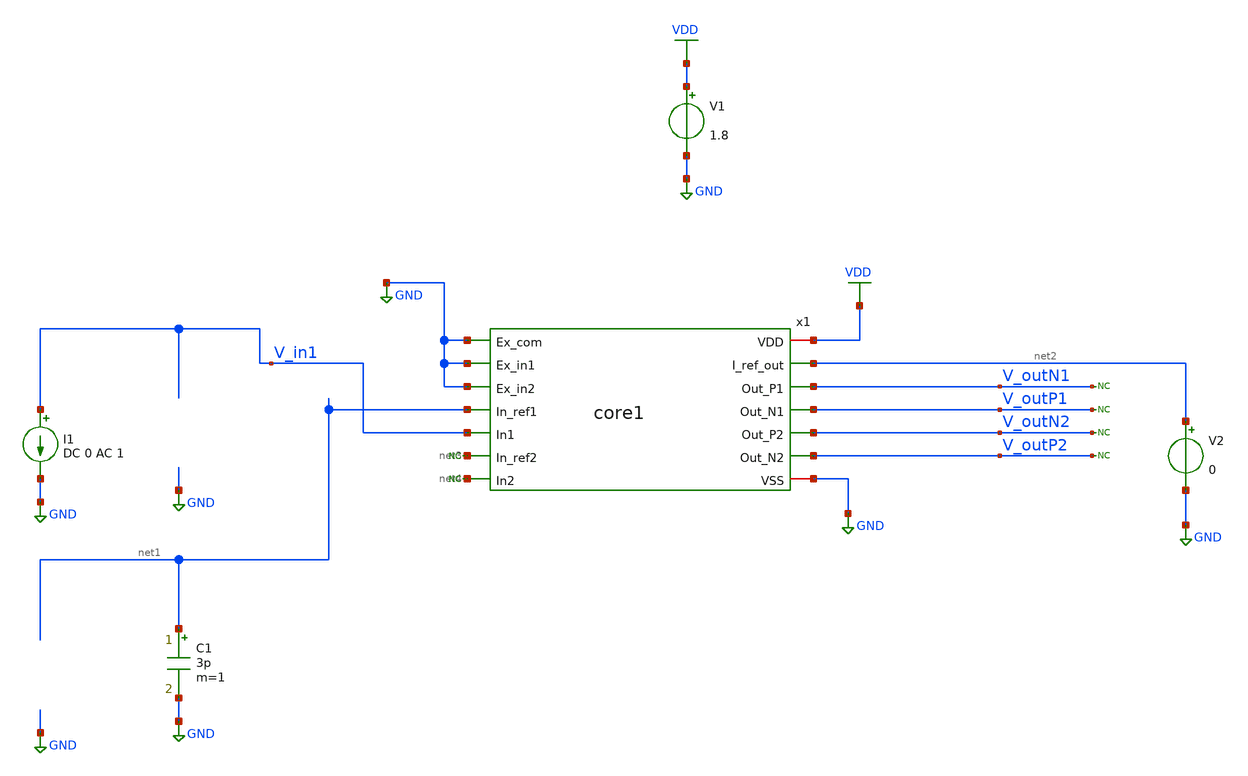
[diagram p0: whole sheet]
** sch_path: xschem/test_core1.sch
**.subckt test_core1
V1 VDD GND 1.8
I1 V_in1 GND DC 0 AC 1
x1 VDD GND GND GND net2 net1 V_outN1 V_in1 V_outP1 net3 V_outN2 net4 V_outP2 GND core1
C1 net1 GND 3p m=1
V2 net2 GND 0
* noconn V_outN1
* noconn V_outP1
* noconn V_outN2
* noconn V_outP2
* noconn #net4
* noconn #net3
**** begin user architecture code


*.options savecurrents
.option warn=1
.option temp=20
.control
set wr_vecnames
set wr_singlescale
set hcopydevtype=svg
** TIA



* save @m.xtia.xm1.msky130_fd_pr__nfet_01v8_lvt[gm]
* save @m.xtia.xm7.msky130_fd_pr__nfet_01v8_lvt[gm]
* save @m.xtia.xm17.msky130_fd_pr__nfet_01v8_lvt[gm]
* save @m.xtia.xm16.msky130_fd_pr__pfet_01v8[gm]
* save @m.xtia.xm8.msky130_fd_pr__pfet_01v8[gm]

* save @m.xtia.xm7.msky130_fd_pr__nfet_01v8_lvt[gm]
* save @m.xtia.xm8.msky130_fd_pr__pfet_01v8[gm]
save all
op

run
write test_core1.raw
reset
save all
ac dec 10 10 1T
plot v(V_in1)
plot v(V_in2)


plot db(v(V_outP1)-v(V_outN1))
*plot db(v(V_outP2)-v(V_outN2))


*meas ac gain FIND vdb(vtia_outp_1) AT=10MEG
*meas ac max_gain max vdb(vtia_outp_1) from=1MEG to=100G
*meas ac min_gain min vdb(vtia_outp_1) from=1MEG to=100MEG
*let bw_gain=gain-3
*meas ac bandwidth when vdb(vtia_outp_1)=bw_gain fall = LAST
*wrdata result_ac_tia.csv gain max_gain min_gain bandwidth


noise v(V_outP1, V_outN1) i1 dec 10 10 4G
print all
* wrdata result_noise.csv inoise_total onoise_total
setplot noise1
plot inoise_spectrum
plot onoise_spectrum
* hardcopy tia_rgc_inoise_spectrum.svg inoise_spectrum
* hardcopy tia_rgc_onoise_spectrum.svg onoise_spectrum
* plot log(inoise_spectrum)
* write noise_tia2.raw

noise v(V_outP1, V_outN1) i1 dec 10 1MEG 4G
print all
* wrdata result_noise.csv inoise_total onoise_total
setplot noise3
plot inoise_spectrum
plot onoise_spectrum
* hardcopy tia_rgc_inoise_spectrum_zoom.svg inoise_spectrum
* hardcopy tia_rgc_onoise_spectrum_zoom.svg onoise_spectrum
* plot log(inoise_spectrum)
* write noise_tia2.raw

noise v(V_outP1, V_outN1) i1 dec 10 100MEG 1.2G
print all
* wrdata result_noise.csv inoise_total onoise_total
setplot noise3
plot inoise_spectrum
plot onoise_spectrum

.endc




* .include ../../tia.spice
* .include ../../filter_diff.spice
* .include ../../cmm_sense3.spice

.include core1.spice
.include tiaA.spice
.include current_mirror_channel.spice
.include current_mirror_channel_s.spice
.include low_pvt_source.spice
.include outdriver_50ohm.spice



* .lib $::SKYWATER_MODELS/sky130.lib.spice #model#
* .lib $::SKYWATER_MODELS/sky130.lib.spice sf
.lib $::SKYWATER_MODELS/sky130.lib.spice.tt.red tt

**** end user architecture code
**.ends

* expanding   symbol:  core1.sym # of pins=14
** sym_path: xschem/core1.sym
** sch_path: xschem/core1.sch
.subckt core1 VDD Ex_com Ex_in1 Ex_in2 I_ref_out In_ref1 Out_P1 In1 Out_N1 In_ref2 Out_P2 In2 Out_N2
+ VSS
*.ipin In_ref1
*.iopin VDD
*.opin Out_N1
*.iopin VSS
*.ipin In2
*.opin Out_P1
*.opin Out_N2
*.opin Out_P2
*.opin I_ref_out
*.ipin In1
*.ipin In_ref2
*.ipin Ex_com
*.ipin Ex_in1
*.ipin Ex_in2
x1 VDD Out_P1 Out_N1 bias_outd_1 tia_out1 tia_ref_out1 VSS outdriver_50ohm
x2 net6 tia_out1 tia_filt_out1 net2 net3 tia_filt_out1 tia_ref_out1 bias_tia_1 VSS tiaA
x3 VDD tia_out2 tia_filt_out2 net4 net5 tia_filt_out2 tia_ref_out2 bias_tia_2 VSS tiaA
x4 VDD Out_P2 Out_N2 bias_outd_2 tia_out2 tia_ref_out2 VSS outdriver_50ohm
x5 VDD is_out bias_outd_2 I_ref_out bias_tia_2 current_mirror_channel_s
x6 VDD is_out bias_outd_1 net1 bias_tia_1 current_mirror_channel
x7 VDD is_out VSS low_pvt_source
* noconn #net1
R1 net2 In_ref1 sky130_fd_pr__res_generic_m5 W=20 L=5 m=1
R2 In1 net3 sky130_fd_pr__res_generic_m5 W=20 L=5 m=1
R3 net4 In_ref2 sky130_fd_pr__res_generic_m5 W=20 L=5 m=1
R4 In2 net5 sky130_fd_pr__res_generic_m5 W=20 L=5 m=1
V1 VDD net6 0
.ends


* expanding   symbol:  outdriver/outdriver_50ohm.sym # of pins=7
** sym_path: xschem/outdriver/outdriver_50ohm.sym
** sch_path: xschem/outdriver/outdriver_50ohm.sch
.subckt outdriver_50ohm VP OutP OutN I_Bias InputSignal InputRef VN
*.iopin VN
*.ipin InputRef
*.iopin VP
*.ipin I_Bias
*.ipin InputSignal
*.opin OutN
*.opin OutP
XM17 net1 VM18D VN VN sky130_fd_pr__nfet_01v8_lvt L=0.3 W=2 nf=1 ad='int((nf+1)/2) * W/nf * 0.29' as='int((nf+2)/2) * W/nf * 0.29'
+ pd='2*int((nf+1)/2) * (W/nf + 0.29)' ps='2*int((nf+2)/2) * (W/nf + 0.29)' nrd='0.29 / W' nrs='0.29 / W'
+ sa=0 sb=0 sd=0 mult=6 m=6
XM18 VM18D VM18D net1 VN sky130_fd_pr__nfet_01v8_lvt L=0.15 W=2 nf=1 ad='int((nf+1)/2) * W/nf * 0.29'
+ as='int((nf+2)/2) * W/nf * 0.29' pd='2*int((nf+1)/2) * (W/nf + 0.29)' ps='2*int((nf+2)/2) * (W/nf + 0.29)'
+ nrd='0.29 / W' nrs='0.29 / W' sa=0 sb=0 sd=0 mult=12 m=12
XM7 I_Bias I_Bias VM18D VM18D sky130_fd_pr__nfet_01v8_lvt L=0.15 W=2 nf=1 ad='int((nf+1)/2) * W/nf * 0.29'
+ as='int((nf+2)/2) * W/nf * 0.29' pd='2*int((nf+1)/2) * (W/nf + 0.29)' ps='2*int((nf+2)/2) * (W/nf + 0.29)'
+ nrd='0.29 / W' nrs='0.29 / W' sa=0 sb=0 sd=0 mult=20 m=20
XM5 VM5D net2 net3 VN sky130_fd_pr__nfet_01v8_lvt L=0.15 W=2 nf=1 ad='int((nf+1)/2) * W/nf * 0.29' as='int((nf+2)/2) * W/nf * 0.29'
+ pd='2*int((nf+1)/2) * (W/nf + 0.29)' ps='2*int((nf+2)/2) * (W/nf + 0.29)' nrd='0.29 / W' nrs='0.29 / W'
+ sa=0 sb=0 sd=0 mult=12*5 m=12*5
XM8 net3 net2 VN VN sky130_fd_pr__nfet_01v8_lvt L=0.3 W=2 nf=1 ad='int((nf+1)/2) * W/nf * 0.29' as='int((nf+2)/2) * W/nf * 0.29'
+ pd='2*int((nf+1)/2) * (W/nf + 0.29)' ps='2*int((nf+2)/2) * (W/nf + 0.29)' nrd='0.29 / W' nrs='0.29 / W'
+ sa=0 sb=0 sd=0 mult=6*5 m=6*5
XM6 net2 I_Bias VM18D VM18D sky130_fd_pr__nfet_01v8_lvt L=8 W=1 nf=1 ad='int((nf+1)/2) * W/nf * 0.29'
+ as='int((nf+2)/2) * W/nf * 0.29' pd='2*int((nf+1)/2) * (W/nf + 0.29)' ps='2*int((nf+2)/2) * (W/nf + 0.29)'
+ nrd='0.29 / W' nrs='0.29 / W' sa=0 sb=0 sd=0 mult=1 m=1
XC1 VN VP sky130_fd_pr__cap_mim_m3_1 W=15 L=30 MF=1 m=1
XM15 VM15D net2 net4 VN sky130_fd_pr__nfet_01v8_lvt L=0.15 W=2 nf=1 ad='int((nf+1)/2) * W/nf * 0.29'
+ as='int((nf+2)/2) * W/nf * 0.29' pd='2*int((nf+1)/2) * (W/nf + 0.29)' ps='2*int((nf+2)/2) * (W/nf + 0.29)'
+ nrd='0.29 / W' nrs='0.29 / W' sa=0 sb=0 sd=0 mult=34*12 m=34*12
XM16 net4 net2 VN VN sky130_fd_pr__nfet_01v8_lvt L=0.3 W=2 nf=1 ad='int((nf+1)/2) * W/nf * 0.29' as='int((nf+2)/2) * W/nf * 0.29'
+ pd='2*int((nf+1)/2) * (W/nf + 0.29)' ps='2*int((nf+2)/2) * (W/nf + 0.29)' nrd='0.29 / W' nrs='0.29 / W'
+ sa=0 sb=0 sd=0 mult=34*6 m=34*6
XM4 OutN V_da3_N VM15D VN sky130_fd_pr__nfet_01v8_lvt L=0.15 W=2 nf=1 ad='int((nf+1)/2) * W/nf * 0.29'
+ as='int((nf+2)/2) * W/nf * 0.29' pd='2*int((nf+1)/2) * (W/nf + 0.29)' ps='2*int((nf+2)/2) * (W/nf + 0.29)'
+ nrd='0.29 / W' nrs='0.29 / W' sa=0 sb=0 sd=0 mult=40 m=40
XM23 V_da2_P InputSignal VM5D VN sky130_fd_pr__nfet_01v8_lvt L=0.15 W=2 nf=1 ad='int((nf+1)/2) * W/nf * 0.29'
+ as='int((nf+2)/2) * W/nf * 0.29' pd='2*int((nf+1)/2) * (W/nf + 0.29)' ps='2*int((nf+2)/2) * (W/nf + 0.29)'
+ nrd='0.29 / W' nrs='0.29 / W' sa=0 sb=0 sd=0 mult=12 m=12
XM19 OutP V_da3_P VM15D VN sky130_fd_pr__nfet_01v8_lvt L=0.15 W=2 nf=1 ad='int((nf+1)/2) * W/nf * 0.29'
+ as='int((nf+2)/2) * W/nf * 0.29' pd='2*int((nf+1)/2) * (W/nf + 0.29)' ps='2*int((nf+2)/2) * (W/nf + 0.29)'
+ nrd='0.29 / W' nrs='0.29 / W' sa=0 sb=0 sd=0 mult=40 m=40
XM14 V_da2_N InputRef VM5D VN sky130_fd_pr__nfet_01v8_lvt L=0.15 W=2 nf=1 ad='int((nf+1)/2) * W/nf * 0.29'
+ as='int((nf+2)/2) * W/nf * 0.29' pd='2*int((nf+1)/2) * (W/nf + 0.29)' ps='2*int((nf+2)/2) * (W/nf + 0.29)'
+ nrd='0.29 / W' nrs='0.29 / W' sa=0 sb=0 sd=0 mult=12 m=12
XR12 OutN VP VN sky130_fd_pr__res_high_po_1p41 L=4 mult=22 m=22
XR13 OutP VP VN sky130_fd_pr__res_high_po_1p41 L=4 mult=22 m=22
XM1 VM1D net2 net5 VN sky130_fd_pr__nfet_01v8_lvt L=0.15 W=2 nf=1 ad='int((nf+1)/2) * W/nf * 0.29' as='int((nf+2)/2) * W/nf * 0.29'
+ pd='2*int((nf+1)/2) * (W/nf + 0.29)' ps='2*int((nf+2)/2) * (W/nf + 0.29)' nrd='0.29 / W' nrs='0.29 / W'
+ sa=0 sb=0 sd=0 mult=4*12*5 m=4*12*5
XM3 net5 net2 VN VN sky130_fd_pr__nfet_01v8_lvt L=0.3 W=2 nf=1 ad='int((nf+1)/2) * W/nf * 0.29' as='int((nf+2)/2) * W/nf * 0.29'
+ pd='2*int((nf+1)/2) * (W/nf + 0.29)' ps='2*int((nf+2)/2) * (W/nf + 0.29)' nrd='0.29 / W' nrs='0.29 / W'
+ sa=0 sb=0 sd=0 mult=4*6*5 m=4*6*5
XM9 V_da3_P V_da2_P VM1D VN sky130_fd_pr__nfet_01v8_lvt L=0.15 W=2 nf=1 ad='int((nf+1)/2) * W/nf * 0.29'
+ as='int((nf+2)/2) * W/nf * 0.29' pd='2*int((nf+1)/2) * (W/nf + 0.29)' ps='2*int((nf+2)/2) * (W/nf + 0.29)'
+ nrd='0.29 / W' nrs='0.29 / W' sa=0 sb=0 sd=0 mult=40 m=40
XM11 V_da3_N V_da2_N VM1D VN sky130_fd_pr__nfet_01v8_lvt L=0.15 W=2 nf=1 ad='int((nf+1)/2) * W/nf * 0.29'
+ as='int((nf+2)/2) * W/nf * 0.29' pd='2*int((nf+1)/2) * (W/nf + 0.29)' ps='2*int((nf+2)/2) * (W/nf + 0.29)'
+ nrd='0.29 / W' nrs='0.29 / W' sa=0 sb=0 sd=0 mult=40 m=40
XR1 V_da2_P VP VN sky130_fd_pr__res_xhigh_po_1p41 L=2 mult=2*4 m=2*4
XR15 V_da2_N VP VN sky130_fd_pr__res_xhigh_po_1p41 L=2 mult=2*4 m=2*4
XR18 V_da3_P VP VN sky130_fd_pr__res_xhigh_po_1p41 L=2 mult=4*2*4 m=4*2*4
XR21 V_da3_N VP VN sky130_fd_pr__res_xhigh_po_1p41 L=2 mult=4*2*4 m=4*2*4
XC6 VN InputRef sky130_fd_pr__cap_mim_m3_1 W=10 L=6 MF=1 m=1
XC2 VN VP sky130_fd_pr__cap_mim_m3_1 W=15 L=30 MF=1 m=1
XC4 VN VP sky130_fd_pr__cap_mim_m3_1 W=15 L=30 MF=1 m=1
XC3 VN net2 sky130_fd_pr__cap_mim_m3_1 W=10 L=16 MF=1 m=1
.ends


* expanding   symbol:  tia/tiaA.sym # of pins=9
** sym_path: xschem/tia/tiaA.sym
** sch_path: xschem/tia/tiaA.sch
.subckt tiaA VP Out_2 Filter_out_1 Input_ref Input Filter_in_2 Ref_out I_Bias1 VN
*.iopin VN
*.iopin VP
*.opin Out_2
*.ipin I_Bias1
*.ipin Input
*.ipin Input_ref
*.opin Filter_out_1
*.ipin Filter_in_2
*.opin Ref_out
XM7 VM7D Input VN VN sky130_fd_pr__nfet_01v8_lvt L=0.15 W=2 nf=1 ad='int((nf+1)/2) * W/nf * 0.29' as='int((nf+2)/2) * W/nf * 0.29'
+ pd='2*int((nf+1)/2) * (W/nf + 0.29)' ps='2*int((nf+2)/2) * (W/nf + 0.29)' nrd='0.29 / W' nrs='0.29 / W'
+ sa=0 sb=0 sd=0 mult=180 m=180
XM8 net1 Input VP VP sky130_fd_pr__pfet_01v8 L=0.15 W=2 nf=1 ad='int((nf+1)/2) * W/nf * 0.29' as='int((nf+2)/2) * W/nf * 0.29'
+ pd='2*int((nf+1)/2) * (W/nf + 0.29)' ps='2*int((nf+2)/2) * (W/nf + 0.29)' nrd='0.29 / W' nrs='0.29 / W'
+ sa=0 sb=0 sd=0 mult=40 m=40
XC4 VN VM9G sky130_fd_pr__cap_mim_m3_1 W=15 L=20 MF=1 m=1
XM18 I_Bias1 I_Bias1 VM10G VN sky130_fd_pr__nfet_01v8_lvt L=0.15 W=2 nf=1 ad='int((nf+1)/2) * W/nf * 0.29'
+ as='int((nf+2)/2) * W/nf * 0.29' pd='2*int((nf+1)/2) * (W/nf + 0.29)' ps='2*int((nf+2)/2) * (W/nf + 0.29)'
+ nrd='0.29 / W' nrs='0.29 / W' sa=0 sb=0 sd=0 mult=30 m=30
XM10 VM10G VM10G VM6D VN sky130_fd_pr__nfet_01v8_lvt L=0.15 W=2 nf=1 ad='int((nf+1)/2) * W/nf * 0.29'
+ as='int((nf+2)/2) * W/nf * 0.29' pd='2*int((nf+1)/2) * (W/nf + 0.29)' ps='2*int((nf+2)/2) * (W/nf + 0.29)'
+ nrd='0.29 / W' nrs='0.29 / W' sa=0 sb=0 sd=0 mult=30 m=30
XM5 Input VM9G VM5D VN sky130_fd_pr__nfet_01v8_lvt L=0.15 W=2 nf=1 ad='int((nf+1)/2) * W/nf * 0.29' as='int((nf+2)/2) * W/nf * 0.29'
+ pd='2*int((nf+1)/2) * (W/nf + 0.29)' ps='2*int((nf+2)/2) * (W/nf + 0.29)' nrd='0.29 / W' nrs='0.29 / W'
+ sa=0 sb=0 sd=0 mult=120 m=120
XM6 VM6D VM10G VN VN sky130_fd_pr__nfet_01v8_lvt L=1 W=2 nf=1 ad='int((nf+1)/2) * W/nf * 0.29' as='int((nf+2)/2) * W/nf * 0.29'
+ pd='2*int((nf+1)/2) * (W/nf + 0.29)' ps='2*int((nf+2)/2) * (W/nf + 0.29)' nrd='0.29 / W' nrs='0.29 / W'
+ sa=0 sb=0 sd=0 mult=30 m=30
XM14 VM9G I_Bias1 VM10G VN sky130_fd_pr__nfet_01v8_lvt L=8 W=1 nf=1 ad='int((nf+1)/2) * W/nf * 0.29'
+ as='int((nf+2)/2) * W/nf * 0.29' pd='2*int((nf+1)/2) * (W/nf + 0.29)' ps='2*int((nf+2)/2) * (W/nf + 0.29)'
+ nrd='0.29 / W' nrs='0.29 / W' sa=0 sb=0 sd=0 mult=1 m=1
XM1 Out_2 net1 Input Input sky130_fd_pr__nfet_01v8_lvt L=0.15 W=2 nf=1 ad='int((nf+1)/2) * W/nf * 0.29'
+ as='int((nf+2)/2) * W/nf * 0.29' pd='2*int((nf+1)/2) * (W/nf + 0.29)' ps='2*int((nf+2)/2) * (W/nf + 0.29)'
+ nrd='0.29 / W' nrs='0.29 / W' sa=0 sb=0 sd=0 mult=60 m=60
XM3 VM5D VM9G VN VN sky130_fd_pr__nfet_01v8_lvt L=1 W=2 nf=1 ad='int((nf+1)/2) * W/nf * 0.29' as='int((nf+2)/2) * W/nf * 0.29'
+ pd='2*int((nf+1)/2) * (W/nf + 0.29)' ps='2*int((nf+2)/2) * (W/nf + 0.29)' nrd='0.29 / W' nrs='0.29 / W'
+ sa=0 sb=0 sd=0 mult=120 m=120
XR1 Out_2 VP VN sky130_fd_pr__res_xhigh_po_1p41 L=4 mult=6 m=6
XM2 VM2D Input_ref VN VN sky130_fd_pr__nfet_01v8_lvt L=0.15 W=2 nf=1 ad='int((nf+1)/2) * W/nf * 0.29'
+ as='int((nf+2)/2) * W/nf * 0.29' pd='2*int((nf+1)/2) * (W/nf + 0.29)' ps='2*int((nf+2)/2) * (W/nf + 0.29)'
+ nrd='0.29 / W' nrs='0.29 / W' sa=0 sb=0 sd=0 mult=180 m=180
XM4 net3 Input_ref VP VP sky130_fd_pr__pfet_01v8 L=0.15 W=2 nf=1 ad='int((nf+1)/2) * W/nf * 0.29' as='int((nf+2)/2) * W/nf * 0.29'
+ pd='2*int((nf+1)/2) * (W/nf + 0.29)' ps='2*int((nf+2)/2) * (W/nf + 0.29)' nrd='0.29 / W' nrs='0.29 / W'
+ sa=0 sb=0 sd=0 mult=40 m=40
XM11 Input_ref VM9G VM15D VN sky130_fd_pr__nfet_01v8_lvt L=0.15 W=2 nf=1 ad='int((nf+1)/2) * W/nf * 0.29'
+ as='int((nf+2)/2) * W/nf * 0.29' pd='2*int((nf+1)/2) * (W/nf + 0.29)' ps='2*int((nf+2)/2) * (W/nf + 0.29)'
+ nrd='0.29 / W' nrs='0.29 / W' sa=0 sb=0 sd=0 mult=120 m=120
XM12 net2 net3 Input_ref Input_ref sky130_fd_pr__nfet_01v8_lvt L=0.15 W=2 nf=1 ad='int((nf+1)/2) * W/nf * 0.29'
+ as='int((nf+2)/2) * W/nf * 0.29' pd='2*int((nf+1)/2) * (W/nf + 0.29)' ps='2*int((nf+2)/2) * (W/nf + 0.29)'
+ nrd='0.29 / W' nrs='0.29 / W' sa=0 sb=0 sd=0 mult=60 m=60
XM15 VM15D VM9G VN VN sky130_fd_pr__nfet_01v8_lvt L=1 W=2 nf=1 ad='int((nf+1)/2) * W/nf * 0.29' as='int((nf+2)/2) * W/nf * 0.29'
+ pd='2*int((nf+1)/2) * (W/nf + 0.29)' ps='2*int((nf+2)/2) * (W/nf + 0.29)' nrd='0.29 / W' nrs='0.29 / W'
+ sa=0 sb=0 sd=0 mult=120 m=120
XR2 net2 VP VN sky130_fd_pr__res_xhigh_po_1p41 L=4 mult=6 m=6
XC5 VN VP sky130_fd_pr__cap_mim_m3_1 W=15 L=30 MF=1 m=1
XC1 VN VP sky130_fd_pr__cap_mim_m3_1 W=15 L=30 MF=1 m=1
XC2 VN Filter_out_1 sky130_fd_pr__cap_mim_m3_1 W=30 L=10 MF=1 m=1
XM29 VM29D VM9G VM33D VN sky130_fd_pr__nfet_01v8_lvt L=0.15 W=2 nf=1 ad='int((nf+1)/2) * W/nf * 0.29'
+ as='int((nf+2)/2) * W/nf * 0.29' pd='2*int((nf+1)/2) * (W/nf + 0.29)' ps='2*int((nf+2)/2) * (W/nf + 0.29)'
+ nrd='0.29 / W' nrs='0.29 / W' sa=0 sb=0 sd=0 mult=20 m=20
XM33 VM33D VM9G VN VN sky130_fd_pr__nfet_01v8_lvt L=1 W=2 nf=1 ad='int((nf+1)/2) * W/nf * 0.29' as='int((nf+2)/2) * W/nf * 0.29'
+ pd='2*int((nf+1)/2) * (W/nf + 0.29)' ps='2*int((nf+2)/2) * (W/nf + 0.29)' nrd='0.29 / W' nrs='0.29 / W'
+ sa=0 sb=0 sd=0 mult=20 m=20
XR3 VM21D VP VN sky130_fd_pr__res_xhigh_po_1p41 L=4 mult=1 m=1
XM21 VM29D VM29D VM21D VP sky130_fd_pr__pfet_01v8 L=0.15 W=2 nf=1 ad='int((nf+1)/2) * W/nf * 0.29' as='int((nf+2)/2) * W/nf * 0.29'
+ pd='2*int((nf+1)/2) * (W/nf + 0.29)' ps='2*int((nf+2)/2) * (W/nf + 0.29)' nrd='0.29 / W' nrs='0.29 / W'
+ sa=0 sb=0 sd=0 mult=10 m=10
XM13 Filter_out_1 VM29D net2 VP sky130_fd_pr__pfet_01v8 L=8 W=1 nf=1 ad='int((nf+1)/2) * W/nf * 0.29'
+ as='int((nf+2)/2) * W/nf * 0.29' pd='2*int((nf+1)/2) * (W/nf + 0.29)' ps='2*int((nf+2)/2) * (W/nf + 0.29)'
+ nrd='0.29 / W' nrs='0.29 / W' sa=0 sb=0 sd=0 mult=1 m=1
XM24 VM24D Input_ref VN VN sky130_fd_pr__nfet_01v8_lvt L=0.15 W=2 nf=1 ad='int((nf+1)/2) * W/nf * 0.29'
+ as='int((nf+2)/2) * W/nf * 0.29' pd='2*int((nf+1)/2) * (W/nf + 0.29)' ps='2*int((nf+2)/2) * (W/nf + 0.29)'
+ nrd='0.29 / W' nrs='0.29 / W' sa=0 sb=0 sd=0 mult=20 m=20
XM30 VM30D VM9G VM31D VN sky130_fd_pr__nfet_01v8_lvt L=0.15 W=2 nf=1 ad='int((nf+1)/2) * W/nf * 0.29'
+ as='int((nf+2)/2) * W/nf * 0.29' pd='2*int((nf+1)/2) * (W/nf + 0.29)' ps='2*int((nf+2)/2) * (W/nf + 0.29)'
+ nrd='0.29 / W' nrs='0.29 / W' sa=0 sb=0 sd=0 mult=2*30 m=2*30
XM31 VM31D VM9G VN VN sky130_fd_pr__nfet_01v8_lvt L=1 W=2 nf=1 ad='int((nf+1)/2) * W/nf * 0.29' as='int((nf+2)/2) * W/nf * 0.29'
+ pd='2*int((nf+1)/2) * (W/nf + 0.29)' ps='2*int((nf+2)/2) * (W/nf + 0.29)' nrd='0.29 / W' nrs='0.29 / W'
+ sa=0 sb=0 sd=0 mult=2*30 m=2*30
XM28 VM28D VM28D VM24D VN sky130_fd_pr__nfet_01v8_lvt L=0.15 W=2 nf=1 ad='int((nf+1)/2) * W/nf * 0.29'
+ as='int((nf+2)/2) * W/nf * 0.29' pd='2*int((nf+1)/2) * (W/nf + 0.29)' ps='2*int((nf+2)/2) * (W/nf + 0.29)'
+ nrd='0.29 / W' nrs='0.29 / W' sa=0 sb=0 sd=0 mult=7 m=7
XM17 net1 VM28D VM7D VN sky130_fd_pr__nfet_01v8_lvt L=0.15 W=2 nf=1 ad='int((nf+1)/2) * W/nf * 0.29'
+ as='int((nf+2)/2) * W/nf * 0.29' pd='2*int((nf+1)/2) * (W/nf + 0.29)' ps='2*int((nf+2)/2) * (W/nf + 0.29)'
+ nrd='0.29 / W' nrs='0.29 / W' sa=0 sb=0 sd=0 mult=40 m=40
XM9 net3 VM28D VM2D VN sky130_fd_pr__nfet_01v8_lvt L=0.15 W=2 nf=1 ad='int((nf+1)/2) * W/nf * 0.29' as='int((nf+2)/2) * W/nf * 0.29'
+ pd='2*int((nf+1)/2) * (W/nf + 0.29)' ps='2*int((nf+2)/2) * (W/nf + 0.29)' nrd='0.29 / W' nrs='0.29 / W'
+ sa=0 sb=0 sd=0 mult=40 m=40
XC10 VN VM28D sky130_fd_pr__cap_mim_m3_1 W=25 L=10 MF=1 m=1
XC11 VN VM28D sky130_fd_pr__cap_mim_m3_1 W=25 L=10 MF=1 m=1
XM36 VM36D VM30D VP VP sky130_fd_pr__pfet_01v8 L=0.5 W=2 nf=1 ad='int((nf+1)/2) * W/nf * 0.29' as='int((nf+2)/2) * W/nf * 0.29'
+ pd='2*int((nf+1)/2) * (W/nf + 0.29)' ps='2*int((nf+2)/2) * (W/nf + 0.29)' nrd='0.29 / W' nrs='0.29 / W'
+ sa=0 sb=0 sd=0 mult=1*30 m=1*30
XM16 VM16D VM30D VP VP sky130_fd_pr__pfet_01v8 L=0.5 W=2 nf=1 ad='int((nf+1)/2) * W/nf * 0.29' as='int((nf+2)/2) * W/nf * 0.29'
+ pd='2*int((nf+1)/2) * (W/nf + 0.29)' ps='2*int((nf+2)/2) * (W/nf + 0.29)' nrd='0.29 / W' nrs='0.29 / W'
+ sa=0 sb=0 sd=0 mult=4*30 m=4*30
XM19 VM28D VM30D VM16D VP sky130_fd_pr__pfet_01v8 L=0.15 W=2 nf=1 ad='int((nf+1)/2) * W/nf * 0.29' as='int((nf+2)/2) * W/nf * 0.29'
+ pd='2*int((nf+1)/2) * (W/nf + 0.29)' ps='2*int((nf+2)/2) * (W/nf + 0.29)' nrd='0.29 / W' nrs='0.29 / W'
+ sa=0 sb=0 sd=0 mult=4*30 m=4*30
XM20 VM30D VM30D VM36D VP sky130_fd_pr__pfet_01v8 L=0.15 W=2 nf=1 ad='int((nf+1)/2) * W/nf * 0.29' as='int((nf+2)/2) * W/nf * 0.29'
+ pd='2*int((nf+1)/2) * (W/nf + 0.29)' ps='2*int((nf+2)/2) * (W/nf + 0.29)' nrd='0.29 / W' nrs='0.29 / W'
+ sa=0 sb=0 sd=0 mult=1*30 m=1*30
XC8 VN Ref_out sky130_fd_pr__cap_mim_m3_1 W=5 L=2 MF=1 m=1
XR9 Ref_out Filter_in_2 VN sky130_fd_pr__res_xhigh_po_0p69 L=6 mult=1 m=1
XC3 VN VM9G sky130_fd_pr__cap_mim_m3_1 W=15 L=20 MF=1 m=1
.ends


* expanding   symbol:  bias/current_mirror_channel_s.sym # of pins=5
** sym_path: xschem/bias/current_mirror_channel_s.sym
** sch_path: xschem/bias/current_mirror_channel_s.sch
.subckt current_mirror_channel_s VP V_in I_Out_Driver I_out_ref I_Out_TIA
*.ipin V_in
*.iopin VP
*.opin I_Out_TIA
*.opin I_Out_Driver
*.opin I_out_ref
XM13 VM13D V_in VP VP sky130_fd_pr__pfet_01v8 L=1 W=2 nf=1 ad='int((nf+1)/2) * W/nf * 0.29' as='int((nf+2)/2) * W/nf * 0.29'
+ pd='2*int((nf+1)/2) * (W/nf + 0.29)' ps='2*int((nf+2)/2) * (W/nf + 0.29)' nrd='0.29 / W' nrs='0.29 / W'
+ sa=0 sb=0 sd=0 mult=8*16 m=8*16
XM4 I_Out_TIA V_in VM13D VP sky130_fd_pr__pfet_01v8 L=0.15 W=2 nf=1 ad='int((nf+1)/2) * W/nf * 0.29'
+ as='int((nf+2)/2) * W/nf * 0.29' pd='2*int((nf+1)/2) * (W/nf + 0.29)' ps='2*int((nf+2)/2) * (W/nf + 0.29)'
+ nrd='0.29 / W' nrs='0.29 / W' sa=0 sb=0 sd=0 mult=8*16 m=8*16
XM1 VM1D V_in VP VP sky130_fd_pr__pfet_01v8 L=1 W=2 nf=1 ad='int((nf+1)/2) * W/nf * 0.29' as='int((nf+2)/2) * W/nf * 0.29'
+ pd='2*int((nf+1)/2) * (W/nf + 0.29)' ps='2*int((nf+2)/2) * (W/nf + 0.29)' nrd='0.29 / W' nrs='0.29 / W'
+ sa=0 sb=0 sd=0 mult=2*2*8*16 m=2*2*8*16
XM3 I_Out_Driver V_in VM1D VP sky130_fd_pr__pfet_01v8 L=0.15 W=2 nf=1 ad='int((nf+1)/2) * W/nf * 0.29'
+ as='int((nf+2)/2) * W/nf * 0.29' pd='2*int((nf+1)/2) * (W/nf + 0.29)' ps='2*int((nf+2)/2) * (W/nf + 0.29)'
+ nrd='0.29 / W' nrs='0.29 / W' sa=0 sb=0 sd=0 mult=2*2*8*16 m=2*2*8*16
XM5 VM5D V_in VP VP sky130_fd_pr__pfet_01v8 L=1 W=2 nf=1 ad='int((nf+1)/2) * W/nf * 0.29' as='int((nf+2)/2) * W/nf * 0.29'
+ pd='2*int((nf+1)/2) * (W/nf + 0.29)' ps='2*int((nf+2)/2) * (W/nf + 0.29)' nrd='0.29 / W' nrs='0.29 / W'
+ sa=0 sb=0 sd=0 mult=8*16 m=8*16
XM6 I_out_ref V_in VM5D VP sky130_fd_pr__pfet_01v8 L=0.15 W=2 nf=1 ad='int((nf+1)/2) * W/nf * 0.29' as='int((nf+2)/2) * W/nf * 0.29'
+ pd='2*int((nf+1)/2) * (W/nf + 0.29)' ps='2*int((nf+2)/2) * (W/nf + 0.29)' nrd='0.29 / W' nrs='0.29 / W'
+ sa=0 sb=0 sd=0 mult=8*16 m=8*16
.ends


* expanding   symbol:  bias/current_mirror_channel.sym # of pins=5
** sym_path: xschem/bias/current_mirror_channel.sym
** sch_path: xschem/bias/current_mirror_channel.sch
.subckt current_mirror_channel VP I_in I_Out_Driver I_out_ref I_Out_TIA
*.ipin I_in
*.iopin VP
*.opin I_Out_TIA
*.opin I_Out_Driver
*.opin I_out_ref
XM13 VM13D I_in VP VP sky130_fd_pr__pfet_01v8 L=1 W=2 nf=1 ad='int((nf+1)/2) * W/nf * 0.29' as='int((nf+2)/2) * W/nf * 0.29'
+ pd='2*int((nf+1)/2) * (W/nf + 0.29)' ps='2*int((nf+2)/2) * (W/nf + 0.29)' nrd='0.29 / W' nrs='0.29 / W'
+ sa=0 sb=0 sd=0 mult=8*16 m=8*16
XM11 VM11D I_in VP VP sky130_fd_pr__pfet_01v8 L=1 W=2 nf=1 ad='int((nf+1)/2) * W/nf * 0.29' as='int((nf+2)/2) * W/nf * 0.29'
+ pd='2*int((nf+1)/2) * (W/nf + 0.29)' ps='2*int((nf+2)/2) * (W/nf + 0.29)' nrd='0.29 / W' nrs='0.29 / W'
+ sa=0 sb=0 sd=0 mult=16 m=16
XM2 I_in I_in VM11D VP sky130_fd_pr__pfet_01v8 L=0.15 W=2 nf=1 ad='int((nf+1)/2) * W/nf * 0.29' as='int((nf+2)/2) * W/nf * 0.29'
+ pd='2*int((nf+1)/2) * (W/nf + 0.29)' ps='2*int((nf+2)/2) * (W/nf + 0.29)' nrd='0.29 / W' nrs='0.29 / W'
+ sa=0 sb=0 sd=0 mult=16 m=16
XM4 I_Out_TIA I_in VM13D VP sky130_fd_pr__pfet_01v8 L=0.15 W=2 nf=1 ad='int((nf+1)/2) * W/nf * 0.29'
+ as='int((nf+2)/2) * W/nf * 0.29' pd='2*int((nf+1)/2) * (W/nf + 0.29)' ps='2*int((nf+2)/2) * (W/nf + 0.29)'
+ nrd='0.29 / W' nrs='0.29 / W' sa=0 sb=0 sd=0 mult=8*16 m=8*16
XM1 VM1D I_in VP VP sky130_fd_pr__pfet_01v8 L=1 W=2 nf=1 ad='int((nf+1)/2) * W/nf * 0.29' as='int((nf+2)/2) * W/nf * 0.29'
+ pd='2*int((nf+1)/2) * (W/nf + 0.29)' ps='2*int((nf+2)/2) * (W/nf + 0.29)' nrd='0.29 / W' nrs='0.29 / W'
+ sa=0 sb=0 sd=0 mult=2*2*8*16 m=2*2*8*16
XM3 I_Out_Driver I_in VM1D VP sky130_fd_pr__pfet_01v8 L=0.15 W=2 nf=1 ad='int((nf+1)/2) * W/nf * 0.29'
+ as='int((nf+2)/2) * W/nf * 0.29' pd='2*int((nf+1)/2) * (W/nf + 0.29)' ps='2*int((nf+2)/2) * (W/nf + 0.29)'
+ nrd='0.29 / W' nrs='0.29 / W' sa=0 sb=0 sd=0 mult=2*2*8*16 m=2*2*8*16
XM5 VM5D I_in VP VP sky130_fd_pr__pfet_01v8 L=1 W=2 nf=1 ad='int((nf+1)/2) * W/nf * 0.29' as='int((nf+2)/2) * W/nf * 0.29'
+ pd='2*int((nf+1)/2) * (W/nf + 0.29)' ps='2*int((nf+2)/2) * (W/nf + 0.29)' nrd='0.29 / W' nrs='0.29 / W'
+ sa=0 sb=0 sd=0 mult=8*16 m=8*16
XM6 I_out_ref I_in VM5D VP sky130_fd_pr__pfet_01v8 L=0.15 W=2 nf=1 ad='int((nf+1)/2) * W/nf * 0.29' as='int((nf+2)/2) * W/nf * 0.29'
+ pd='2*int((nf+1)/2) * (W/nf + 0.29)' ps='2*int((nf+2)/2) * (W/nf + 0.29)' nrd='0.29 / W' nrs='0.29 / W'
+ sa=0 sb=0 sd=0 mult=8*16 m=8*16
.ends


* expanding   symbol:  bias/low_pvt_source.sym # of pins=3
** sym_path: bias/low_pvt_source.sym
** sch_path: bias/low_pvt_source.sch
.subckt low_pvt_source VP I_ref VN
*.iopin VP
*.opin I_ref
*.iopin VN
XM1 VM1D VM8D VP VP sky130_fd_pr__pfet_01v8 L=1 W=4 nf=1 ad='int((nf+1)/2) * W/nf * 0.29' as='int((nf+2)/2) * W/nf * 0.29'
+ pd='2*int((nf+1)/2) * (W/nf + 0.29)' ps='2*int((nf+2)/2) * (W/nf + 0.29)' nrd='0.29 / W' nrs='0.29 / W'
+ sa=0 sb=0 sd=0 mult=10 m=10
XM2 VM2D VM2D VN VN sky130_fd_pr__nfet_01v8 L=6 W=4 nf=1 ad='int((nf+1)/2) * W/nf * 0.29' as='int((nf+2)/2) * W/nf * 0.29'
+ pd='2*int((nf+1)/2) * (W/nf + 0.29)' ps='2*int((nf+2)/2) * (W/nf + 0.29)' nrd='0.29 / W' nrs='0.29 / W'
+ sa=0 sb=0 sd=0 mult=30 m=30
XM5 VM9D VM8D VM1D VP sky130_fd_pr__pfet_01v8 L=0.2 W=4 nf=1 ad='int((nf+1)/2) * W/nf * 0.29' as='int((nf+2)/2) * W/nf * 0.29'
+ pd='2*int((nf+1)/2) * (W/nf + 0.29)' ps='2*int((nf+2)/2) * (W/nf + 0.29)' nrd='0.29 / W' nrs='0.29 / W'
+ sa=0 sb=0 sd=0 mult=2 m=2
XM11 VM11D VM2D VM12D VN sky130_fd_pr__nfet_01v8 L=6 W=4 nf=1 ad='int((nf+1)/2) * W/nf * 0.29' as='int((nf+2)/2) * W/nf * 0.29'
+ pd='2*int((nf+1)/2) * (W/nf + 0.29)' ps='2*int((nf+2)/2) * (W/nf + 0.29)' nrd='0.29 / W' nrs='0.29 / W'
+ sa=0 sb=0 sd=0 mult=65 m=65
XM12 VM12D VM12G VN VN sky130_fd_pr__nfet_01v8 L=6 W=4 nf=1 ad='int((nf+1)/2) * W/nf * 0.29' as='int((nf+2)/2) * W/nf * 0.29'
+ pd='2*int((nf+1)/2) * (W/nf + 0.29)' ps='2*int((nf+2)/2) * (W/nf + 0.29)' nrd='0.29 / W' nrs='0.29 / W'
+ sa=0 sb=0 sd=0 mult=2 m=2
XM14 VM14D VM12G VN VN sky130_fd_pr__nfet_01v8 L=6 W=4 nf=1 ad='int((nf+1)/2) * W/nf * 0.29' as='int((nf+2)/2) * W/nf * 0.29'
+ pd='2*int((nf+1)/2) * (W/nf + 0.29)' ps='2*int((nf+2)/2) * (W/nf + 0.29)' nrd='0.29 / W' nrs='0.29 / W'
+ sa=0 sb=0 sd=0 mult=2 m=2
XM16 VM16D VM8D VP VP sky130_fd_pr__pfet_01v8 L=1 W=4 nf=1 ad='int((nf+1)/2) * W/nf * 0.29' as='int((nf+2)/2) * W/nf * 0.29'
+ pd='2*int((nf+1)/2) * (W/nf + 0.29)' ps='2*int((nf+2)/2) * (W/nf + 0.29)' nrd='0.29 / W' nrs='0.29 / W'
+ sa=0 sb=0 sd=0 mult=10 m=10
XM17 VM8D VM8D VM16D VP sky130_fd_pr__pfet_01v8 L=0.2 W=4 nf=1 ad='int((nf+1)/2) * W/nf * 0.29' as='int((nf+2)/2) * W/nf * 0.29'
+ pd='2*int((nf+1)/2) * (W/nf + 0.29)' ps='2*int((nf+2)/2) * (W/nf + 0.29)' nrd='0.29 / W' nrs='0.29 / W'
+ sa=0 sb=0 sd=0 mult=2 m=2
XM18 VM18D VM8D VP VP sky130_fd_pr__pfet_01v8 L=1 W=4 nf=1 ad='int((nf+1)/2) * W/nf * 0.29' as='int((nf+2)/2) * W/nf * 0.29'
+ pd='2*int((nf+1)/2) * (W/nf + 0.29)' ps='2*int((nf+2)/2) * (W/nf + 0.29)' nrd='0.29 / W' nrs='0.29 / W'
+ sa=0 sb=0 sd=0 mult=10*3*2 m=10*3*2
XM19 VM14D VM8D VM18D VP sky130_fd_pr__pfet_01v8 L=0.2 W=4 nf=1 ad='int((nf+1)/2) * W/nf * 0.29' as='int((nf+2)/2) * W/nf * 0.29'
+ pd='2*int((nf+1)/2) * (W/nf + 0.29)' ps='2*int((nf+2)/2) * (W/nf + 0.29)' nrd='0.29 / W' nrs='0.29 / W'
+ sa=0 sb=0 sd=0 mult=2*3*2 m=2*3*2
XM20 VM20D VM8D VP VP sky130_fd_pr__pfet_01v8 L=1 W=4 nf=1 ad='int((nf+1)/2) * W/nf * 0.29' as='int((nf+2)/2) * W/nf * 0.29'
+ pd='2*int((nf+1)/2) * (W/nf + 0.29)' ps='2*int((nf+2)/2) * (W/nf + 0.29)' nrd='0.29 / W' nrs='0.29 / W'
+ sa=0 sb=0 sd=0 mult=10*1*1 m=10*1*1
XM21 VM22D VM8D VM20D VP sky130_fd_pr__pfet_01v8 L=0.2 W=4 nf=1 ad='int((nf+1)/2) * W/nf * 0.29' as='int((nf+2)/2) * W/nf * 0.29'
+ pd='2*int((nf+1)/2) * (W/nf + 0.29)' ps='2*int((nf+2)/2) * (W/nf + 0.29)' nrd='0.29 / W' nrs='0.29 / W'
+ sa=0 sb=0 sd=0 mult=2*1*1 m=2*1*1
XM22 VM22D VM4S VM3D VN sky130_fd_pr__nfet_01v8 L=6 W=4 nf=1 ad='int((nf+1)/2) * W/nf * 0.29' as='int((nf+2)/2) * W/nf * 0.29'
+ pd='2*int((nf+1)/2) * (W/nf + 0.29)' ps='2*int((nf+2)/2) * (W/nf + 0.29)' nrd='0.29 / W' nrs='0.29 / W'
+ sa=0 sb=0 sd=0 mult=20 m=20
XM3 VM3D VM3G VN VN sky130_fd_pr__nfet_01v8 L=6 W=4 nf=1 ad='int((nf+1)/2) * W/nf * 0.29' as='int((nf+2)/2) * W/nf * 0.29'
+ pd='2*int((nf+1)/2) * (W/nf + 0.29)' ps='2*int((nf+2)/2) * (W/nf + 0.29)' nrd='0.29 / W' nrs='0.29 / W'
+ sa=0 sb=0 sd=0 mult=4 m=4
XM13 VP VM14D VM12G VM12G sky130_fd_pr__nfet_01v8_lvt L=0.15 W=4 nf=1 ad='int((nf+1)/2) * W/nf * 0.29'
+ as='int((nf+2)/2) * W/nf * 0.29' pd='2*int((nf+1)/2) * (W/nf + 0.29)' ps='2*int((nf+2)/2) * (W/nf + 0.29)'
+ nrd='0.29 / W' nrs='0.29 / W' sa=0 sb=0 sd=0 mult=20 m=20
XM4 I_ref VM22D VM4S VN sky130_fd_pr__nfet_01v8_lvt L=0.15 W=4 nf=1 ad='int((nf+1)/2) * W/nf * 0.29'
+ as='int((nf+2)/2) * W/nf * 0.29' pd='2*int((nf+1)/2) * (W/nf + 0.29)' ps='2*int((nf+2)/2) * (W/nf + 0.29)'
+ nrd='0.29 / W' nrs='0.29 / W' sa=0 sb=0 sd=0 mult=20 m=20
XM48 VM50D VM11D VP VP sky130_fd_pr__pfet_01v8 L=2 W=0.5 nf=1 ad='int((nf+1)/2) * W/nf * 0.29' as='int((nf+2)/2) * W/nf * 0.29'
+ pd='2*int((nf+1)/2) * (W/nf + 0.29)' ps='2*int((nf+2)/2) * (W/nf + 0.29)' nrd='0.29 / W' nrs='0.29 / W'
+ sa=0 sb=0 sd=0 mult=1 m=1
XM50 VM50D VM11D VN VN sky130_fd_pr__nfet_01v8_lvt L=0.2 W=4 nf=1 ad='int((nf+1)/2) * W/nf * 0.29' as='int((nf+2)/2) * W/nf * 0.29'
+ pd='2*int((nf+1)/2) * (W/nf + 0.29)' ps='2*int((nf+2)/2) * (W/nf + 0.29)' nrd='0.29 / W' nrs='0.29 / W'
+ sa=0 sb=0 sd=0 mult=10 m=10
XC3 VP VM8D sky130_fd_pr__cap_mim_m3_1 W=20 L=20 MF=1 m=1
XM8 VM8D VM9D VM11D VM11D sky130_fd_pr__nfet_01v8_lvt L=1 W=4 nf=1 ad='int((nf+1)/2) * W/nf * 0.29' as='int((nf+2)/2) * W/nf * 0.29'
+ pd='2*int((nf+1)/2) * (W/nf + 0.29)' ps='2*int((nf+2)/2) * (W/nf + 0.29)' nrd='0.29 / W' nrs='0.29 / W'
+ sa=0 sb=0 sd=0 mult=20 m=20
XM9 VM9D VM9D VM2D VM2D sky130_fd_pr__nfet_01v8_lvt L=1 W=4 nf=1 ad='int((nf+1)/2) * W/nf * 0.29' as='int((nf+2)/2) * W/nf * 0.29'
+ pd='2*int((nf+1)/2) * (W/nf + 0.29)' ps='2*int((nf+2)/2) * (W/nf + 0.29)' nrd='0.29 / W' nrs='0.29 / W'
+ sa=0 sb=0 sd=0 mult=20 m=20
XM10 VM8D VM50D VN VN sky130_fd_pr__nfet_01v8 L=2 W=0.5 nf=1 ad='int((nf+1)/2) * W/nf * 0.29' as='int((nf+2)/2) * W/nf * 0.29'
+ pd='2*int((nf+1)/2) * (W/nf + 0.29)' ps='2*int((nf+2)/2) * (W/nf + 0.29)' nrd='0.29 / W' nrs='0.29 / W'
+ sa=0 sb=0 sd=0 mult=1 m=1
XR7 net3 VM4S VN sky130_fd_pr__res_xhigh_po_1p41 L=10 mult=1 m=1
XR3 net4 net3 VN sky130_fd_pr__res_xhigh_po_1p41 L=10 mult=1 m=1
XR4 net2 net4 VN sky130_fd_pr__res_xhigh_po_1p41 L=10 mult=1 m=1
XR5 net1 net2 VN sky130_fd_pr__res_xhigh_po_1p41 L=10 mult=1 m=1
XR6 VN net1 VN sky130_fd_pr__res_xhigh_po_1p41 L=10 mult=1 m=1
XR8 net5 VM12G VN sky130_fd_pr__res_xhigh_po_1p41 L=10 mult=1 m=1
XR1 net5 VM3G VN sky130_fd_pr__res_xhigh_po_1p41 L=10 mult=1 m=1
XR2 net7 net6 VN sky130_fd_pr__res_xhigh_po_1p41 L=10 mult=1 m=1
XR9 VN net6 VN sky130_fd_pr__res_xhigh_po_1p41 L=10 mult=1 m=1
XR10 net11 net7 VN sky130_fd_pr__res_xhigh_po_1p41 L=10 mult=1 m=1
XR11 net12 net11 VN sky130_fd_pr__res_xhigh_po_1p41 L=10 mult=1 m=1
XR12 net8 net12 VN sky130_fd_pr__res_xhigh_po_1p41 L=10 mult=1 m=1
XR13 net10 VM3G VN sky130_fd_pr__res_xhigh_po_1p41 L=10 mult=1 m=1
XR14 net9 net10 VN sky130_fd_pr__res_xhigh_po_1p41 L=10 mult=1 m=1
XR15 net8 net9 VN sky130_fd_pr__res_xhigh_po_1p41 L=10 mult=1 m=1
XC2 VP VN sky130_fd_pr__cap_mim_m3_1 W=25 L=30 MF=1 m=1
XC1 VP VN sky130_fd_pr__cap_mim_m3_1 W=25 L=30 MF=1 m=1
.ends

.GLOBAL VDD
.GLOBAL GND
.end
